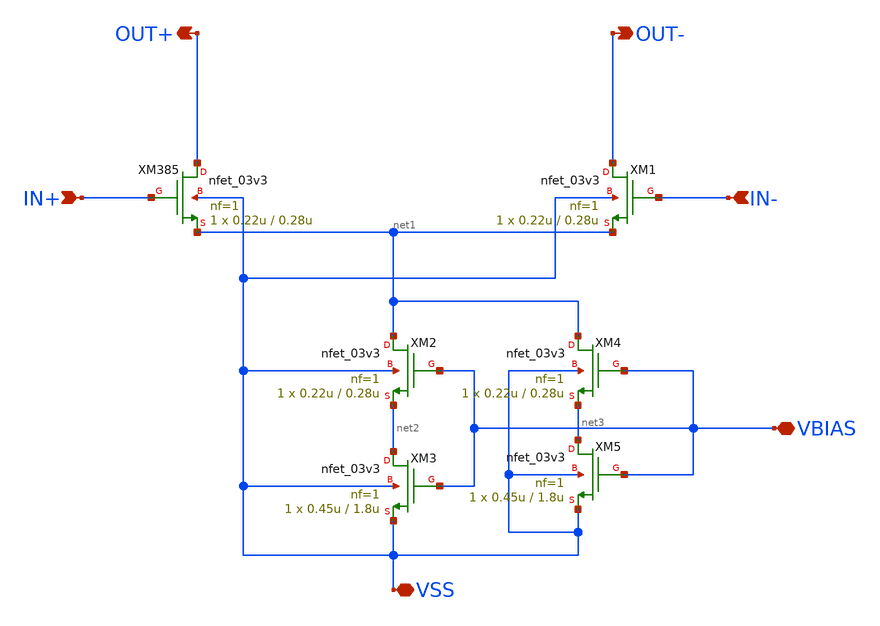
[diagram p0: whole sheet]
** sch_path: xschem/CS_Switch_4x.sch
**.subckt CS_Switch_4x IN+ IN- OUT+ OUT- VBIAS VSS
*.ipin IN+
*.ipin IN-
*.opin OUT+
*.opin OUT-
*.iopin VBIAS
*.iopin VSS
XM385 OUT+ IN+ net1 VSS nfet_03v3 L=0.28u W=0.22u nf=1 ad='int((nf+1)/2) * W/nf * 0.18u' as='int((nf+2)/2) * W/nf * 0.18u'
+ pd='2*int((nf+1)/2) * (W/nf + 0.18u)' ps='2*int((nf+2)/2) * (W/nf + 0.18u)' nrd='0.18u / W' nrs='0.18u / W'
+ sa=0 sb=0 sd=0 m=1
XM2 net1 VBIAS net2 VSS nfet_03v3 L=0.28u W=0.22u nf=1 ad='int((nf+1)/2) * W/nf * 0.18u' as='int((nf+2)/2) * W/nf * 0.18u'
+ pd='2*int((nf+1)/2) * (W/nf + 0.18u)' ps='2*int((nf+2)/2) * (W/nf + 0.18u)' nrd='0.18u / W' nrs='0.18u / W'
+ sa=0 sb=0 sd=0 m=1
XM1 OUT- IN- net1 VSS nfet_03v3 L=0.28u W=0.22u nf=1 ad='int((nf+1)/2) * W/nf * 0.18u' as='int((nf+2)/2) * W/nf * 0.18u'
+ pd='2*int((nf+1)/2) * (W/nf + 0.18u)' ps='2*int((nf+2)/2) * (W/nf + 0.18u)' nrd='0.18u / W' nrs='0.18u / W'
+ sa=0 sb=0 sd=0 m=1
XM4 net1 VBIAS net3 VSS nfet_03v3 L=0.28u W=0.22u nf=1 ad='int((nf+1)/2) * W/nf * 0.18u' as='int((nf+2)/2) * W/nf * 0.18u'
+ pd='2*int((nf+1)/2) * (W/nf + 0.18u)' ps='2*int((nf+2)/2) * (W/nf + 0.18u)' nrd='0.18u / W' nrs='0.18u / W'
+ sa=0 sb=0 sd=0 m=1
XM5 net3 VBIAS VSS VSS nfet_03v3 L=1.8u W=0.45u nf=1 ad='int((nf+1)/2) * W/nf * 0.18u' as='int((nf+2)/2) * W/nf * 0.18u'
+ pd='2*int((nf+1)/2) * (W/nf + 0.18u)' ps='2*int((nf+2)/2) * (W/nf + 0.18u)' nrd='0.18u / W' nrs='0.18u / W'
+ sa=0 sb=0 sd=0 m=1
XM3 net2 VBIAS VSS VSS nfet_03v3 L=1.8u W=0.45u nf=1 ad='int((nf+1)/2) * W/nf * 0.18u' as='int((nf+2)/2) * W/nf * 0.18u'
+ pd='2*int((nf+1)/2) * (W/nf + 0.18u)' ps='2*int((nf+2)/2) * (W/nf + 0.18u)' nrd='0.18u / W' nrs='0.18u / W'
+ sa=0 sb=0 sd=0 m=1
**.ends
.end
